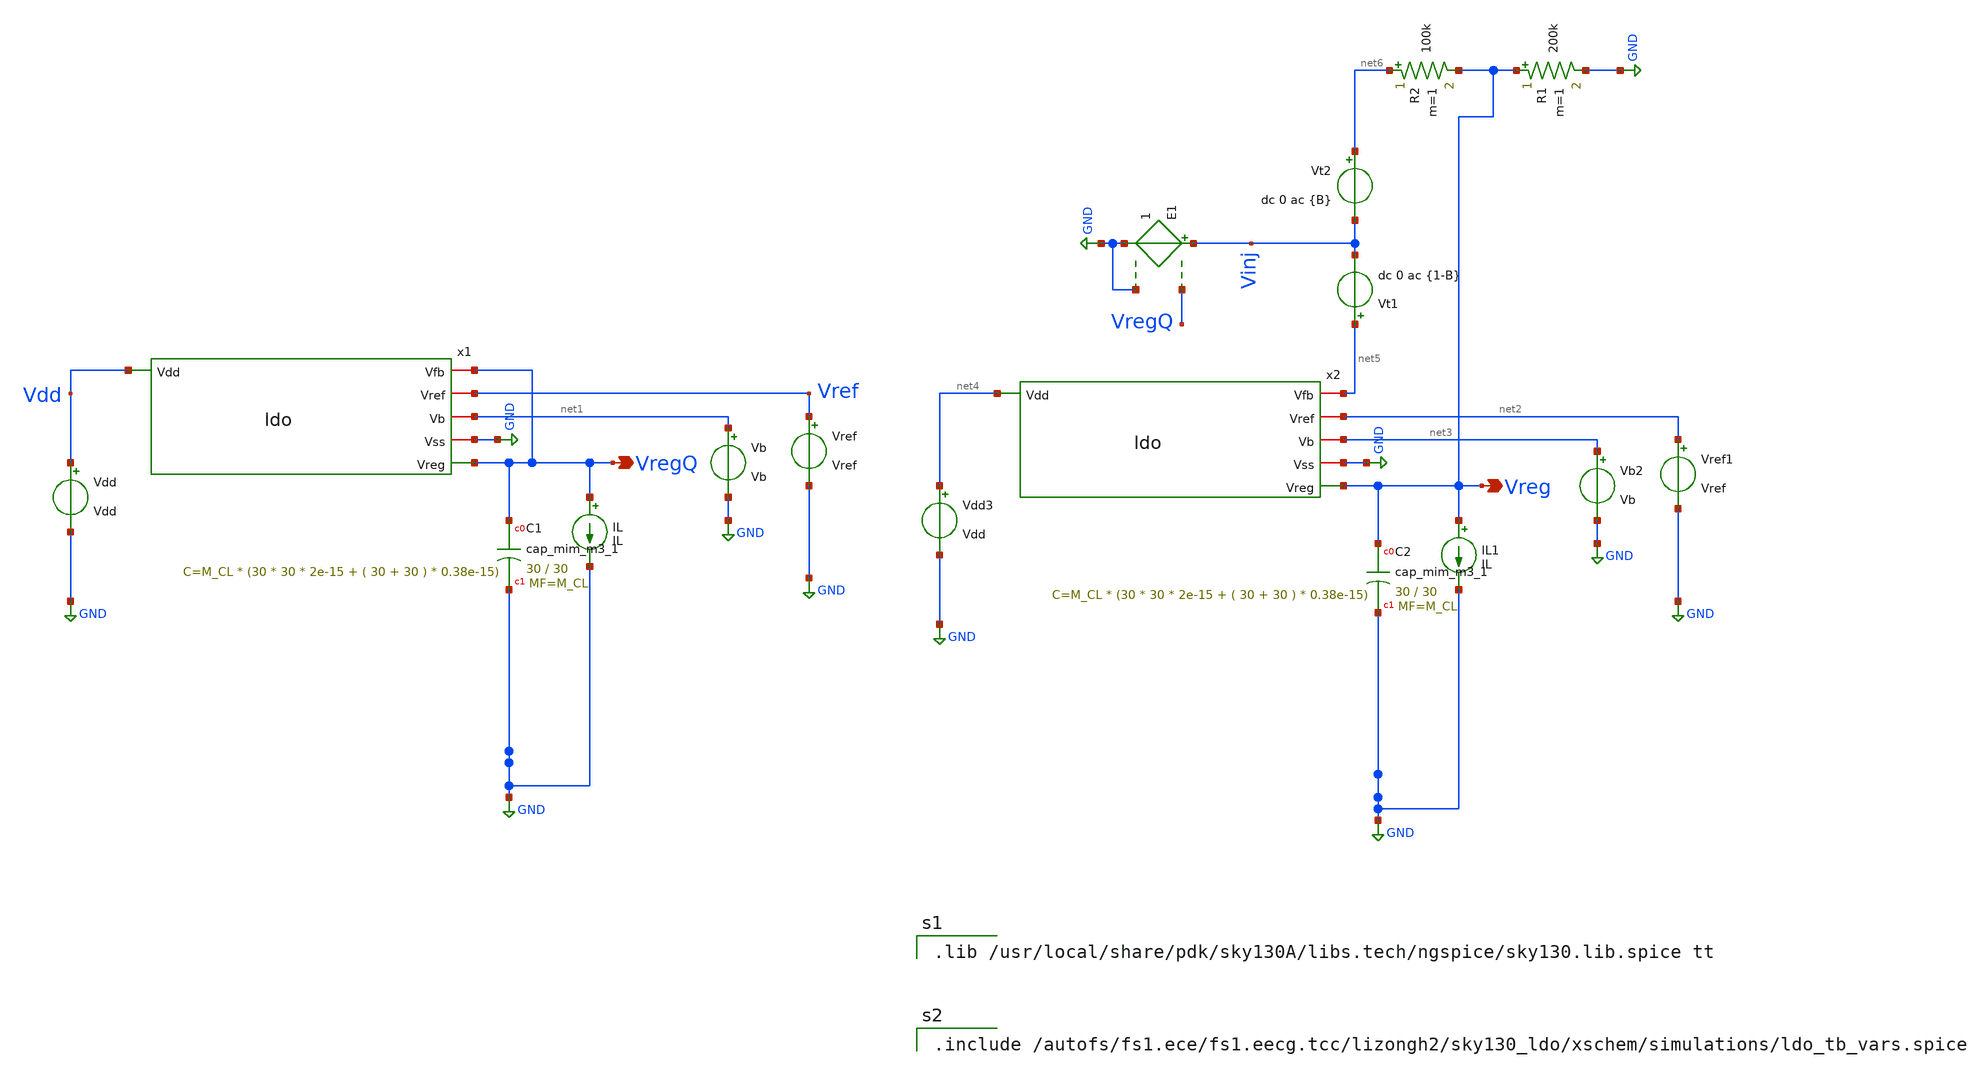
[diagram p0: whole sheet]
** sch_path: xschem/ldo_tb_stb.sch
**.subckt ldo_tb_stb VregQ Vreg
*.opin VregQ
*.opin Vreg
Vref Vref GND Vref
Vb net1 GND Vb
IL VregQ GND IL
Vdd Vdd GND Vdd
x1 Vdd VregQ Vref net1 GND VregQ ldo
Vref1 net2 GND Vref
Vb2 net3 GND Vb
IL1 Vreg GND IL
Vdd3 net4 GND Vdd
x2 net4 net5 net2 net3 GND Vreg ldo
Vt1 net5 Vinj dc 0 ac {1-B}
Vt2 net6 Vinj dc 0 ac {B}
E1 Vinj GND VregQ GND 1
XC1 VregQ GND sky130_fd_pr__cap_mim_m3_1 W=30 L=30 MF=M_CL m=M_CL
XC2 Vreg GND sky130_fd_pr__cap_mim_m3_1 W=30 L=30 MF=M_CL m=M_CL
R1 Vreg GND 200k m=1
R2 net6 Vreg 100k m=1
**** begin user architecture code

.lib /usr/local/share/pdk/sky130A/libs.tech/ngspice/sky130.lib.spice tt



.control
save all
set filetype=ascii
set units=degrees

* Stability_Analysis using Ochoa's Z method
alter IL dc=100u
.param B=0
ac dec 10 1 10G
alterparam B=1
reset
ac dec 10 1 10G
let L = (ac1.i(Vt2) + ac2.i(Vt1)) / (ac1.i(Vt1) + ac2.i(Vt2))
let Lmag = db(L)
let Lph = vp(L)
plot Lmag Lph xlog
wrdata ldo_tb_loop_gain mag(L) vp(L)

.endc



.include /autofs/fs1.ece/fs1.eecg.tcc/lizongh2/sky130_ldo/xschem/simulations/ldo_tb_vars.spice


**** end user architecture code
**.ends

* expanding   symbol:  ldo.sym # of pins=6
** sym_path: xschem/ldo.sym
** sch_path: xschem/ldo.sch
.subckt ldo Vdd Vfb Vref Vb Vss Vreg
*.iopin Vb
*.iopin Vss
*.opin Vreg
*.iopin Vref
*.ipin Vdd
*.iopin Vfb
x1 Vdd net1 Vfb Vref Vb Vss diff_pair
XM6 Vreg net1 Vdd Vdd sky130_fd_pr__pfet_g5v0d10v5 L=L_pass W=W_pass nf=Nf_pass ad='int((nf+1)/2) * W/nf
+ * 0.29' as='int((nf+2)/2) * W/nf * 0.29' pd='2*int((nf+1)/2) * (W/nf + 0.29)' ps='2*int((nf+2)/2) * (W/nf
+ + 0.29)' nrd='0.29 / W' nrs='0.29 / W' sa=0 sb=0 sd=0 mult=M_pass m=M_pass
XCfb net2 Vreg sky130_fd_pr__cap_mim_m3_1 W=10 L=10 MF=M_Cfb m=M_Cfb
XRfb net2 net1 Vss sky130_fd_pr__res_high_po_0p35 L=3 mult=M_Rfb m=M_Rfb
.ends


* expanding   symbol:  diff_pair.sym # of pins=6
** sym_path: xschem/diff_pair.sym
** sch_path: xschem/diff_pair.sch
.subckt diff_pair Vdd vout vinp vinm Vb Vss
*.iopin Vdd
*.ipin vinm
*.ipin vinp
*.iopin Vb
*.opin vout
*.iopin Vss
XM1 net1 vinp net2 Vss sky130_fd_pr__nfet_g5v0d10v5 L=L_M1 W=W_M1 nf=1 ad='int((nf+1)/2) * W/nf * 0.29' as='int((nf+2)/2)
+ * W/nf * 0.29' pd='2*int((nf+1)/2) * (W/nf + 0.29)' ps='2*int((nf+2)/2) * (W/nf + 0.29)' nrd='0.29 /
+ W' nrs='0.29 / W' sa=0 sb=0 sd=0 mult=1 m=1
XM2 vout vinm net2 Vss sky130_fd_pr__nfet_g5v0d10v5 L=L_M2 W=W_M2 nf=1 ad='int((nf+1)/2) * W/nf * 0.29' as='int((nf+2)/2)
+ * W/nf * 0.29' pd='2*int((nf+1)/2) * (W/nf + 0.29)' ps='2*int((nf+2)/2) * (W/nf + 0.29)' nrd='0.29 /
+ W' nrs='0.29 / W' sa=0 sb=0 sd=0 mult=1 m=1
XM3 vout net1 Vdd Vdd sky130_fd_pr__pfet_g5v0d10v5 L=L_M3 W=W_M3 nf=1 ad='int((nf+1)/2) * W/nf * 0.29' as='int((nf+2)/2)
+ * W/nf * 0.29' pd='2*int((nf+1)/2) * (W/nf + 0.29)' ps='2*int((nf+2)/2) * (W/nf + 0.29)' nrd='0.29 /
+ W' nrs='0.29 / W' sa=0 sb=0 sd=0 mult=1 m=1
XM4 net1 net1 Vdd Vdd sky130_fd_pr__pfet_g5v0d10v5 L=L_M4 W=W_M4 nf=1 ad='int((nf+1)/2) * W/nf * 0.29' as='int((nf+2)/2)
+ * W/nf * 0.29' pd='2*int((nf+1)/2) * (W/nf + 0.29)' ps='2*int((nf+2)/2) * (W/nf + 0.29)' nrd='0.29 /
+ W' nrs='0.29 / W' sa=0 sb=0 sd=0 mult=1 m=1
XM5 net2 Vb Vss Vss sky130_fd_pr__nfet_g5v0d10v5 L=L_M5 W=W_M5 nf=1 ad='int((nf+1)/2) * W/nf * 0.29' as='int((nf+2)/2)
+ * W/nf * 0.29' pd='2*int((nf+1)/2) * (W/nf + 0.29)' ps='2*int((nf+2)/2) * (W/nf + 0.29)' nrd='0.29 /
+ W' nrs='0.29 / W' sa=0 sb=0 sd=0 mult=1 m=1
.ends

.GLOBAL GND
.end
